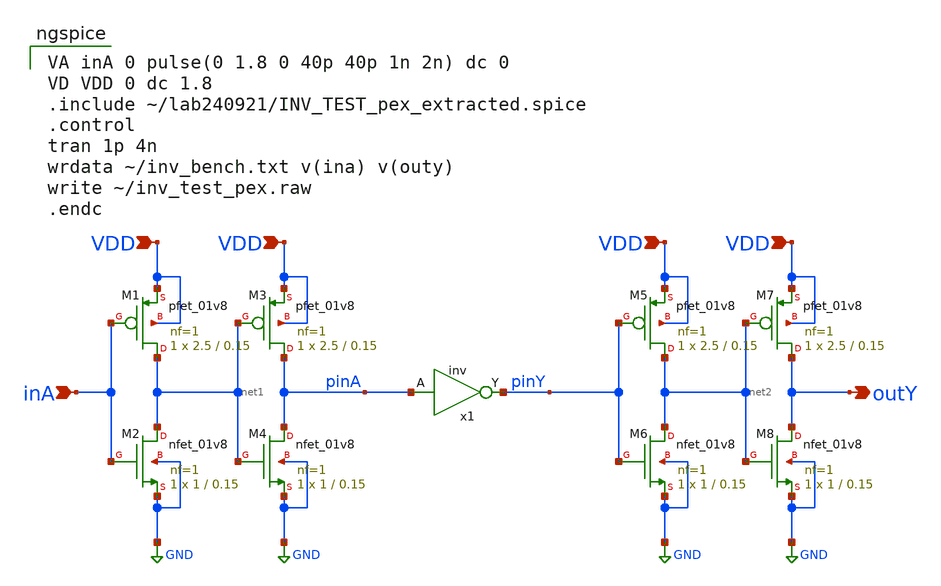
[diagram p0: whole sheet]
** sch_path: inv_pex.sch
**.subckt inv_pex inA VDD VDD VDD VDD outY
*.ipin inA
*.ipin VDD
*.ipin VDD
*.ipin VDD
*.ipin VDD
*.opin outY
XM1 net1 inA VDD VDD sky130_fd_pr__pfet_01v8 L=0.15 W=2.5 nf=1 ad='int((nf+1)/2) * W/nf * 0.29' as='int((nf+2)/2) * W/nf * 0.29'
+ pd='2*int((nf+1)/2) * (W/nf + 0.29)' ps='2*int((nf+2)/2) * (W/nf + 0.29)' nrd='0.29 / W' nrs='0.29 / W'
+ sa=0 sb=0 sd=0 mult=1 m=1
XM2 net1 inA GND GND sky130_fd_pr__nfet_01v8 L=0.15 W=1 nf=1 ad='int((nf+1)/2) * W/nf * 0.29' as='int((nf+2)/2) * W/nf * 0.29'
+ pd='2*int((nf+1)/2) * (W/nf + 0.29)' ps='2*int((nf+2)/2) * (W/nf + 0.29)' nrd='0.29 / W' nrs='0.29 / W'
+ sa=0 sb=0 sd=0 mult=1 m=1
x1 pinA pinY VDD GND INV_TEST
XM3 pinA net1 VDD VDD sky130_fd_pr__pfet_01v8 L=0.15 W=2.5 nf=1 ad='int((nf+1)/2) * W/nf * 0.29' as='int((nf+2)/2) * W/nf * 0.29'
+ pd='2*int((nf+1)/2) * (W/nf + 0.29)' ps='2*int((nf+2)/2) * (W/nf + 0.29)' nrd='0.29 / W' nrs='0.29 / W'
+ sa=0 sb=0 sd=0 mult=1 m=1
XM4 pinA net1 GND GND sky130_fd_pr__nfet_01v8 L=0.15 W=1 nf=1 ad='int((nf+1)/2) * W/nf * 0.29' as='int((nf+2)/2) * W/nf * 0.29'
+ pd='2*int((nf+1)/2) * (W/nf + 0.29)' ps='2*int((nf+2)/2) * (W/nf + 0.29)' nrd='0.29 / W' nrs='0.29 / W'
+ sa=0 sb=0 sd=0 mult=1 m=1
XM5 net2 pinY VDD VDD sky130_fd_pr__pfet_01v8 L=0.15 W=2.5 nf=1 ad='int((nf+1)/2) * W/nf * 0.29' as='int((nf+2)/2) * W/nf * 0.29'
+ pd='2*int((nf+1)/2) * (W/nf + 0.29)' ps='2*int((nf+2)/2) * (W/nf + 0.29)' nrd='0.29 / W' nrs='0.29 / W'
+ sa=0 sb=0 sd=0 mult=1 m=1
XM6 net2 pinY GND GND sky130_fd_pr__nfet_01v8 L=0.15 W=1 nf=1 ad='int((nf+1)/2) * W/nf * 0.29' as='int((nf+2)/2) * W/nf * 0.29'
+ pd='2*int((nf+1)/2) * (W/nf + 0.29)' ps='2*int((nf+2)/2) * (W/nf + 0.29)' nrd='0.29 / W' nrs='0.29 / W'
+ sa=0 sb=0 sd=0 mult=1 m=1
XM7 outY net2 VDD VDD sky130_fd_pr__pfet_01v8 L=0.15 W=2.5 nf=1 ad='int((nf+1)/2) * W/nf * 0.29' as='int((nf+2)/2) * W/nf * 0.29'
+ pd='2*int((nf+1)/2) * (W/nf + 0.29)' ps='2*int((nf+2)/2) * (W/nf + 0.29)' nrd='0.29 / W' nrs='0.29 / W'
+ sa=0 sb=0 sd=0 mult=1 m=1
XM8 outY net2 GND GND sky130_fd_pr__nfet_01v8 L=0.15 W=1 nf=1 ad='int((nf+1)/2) * W/nf * 0.29' as='int((nf+2)/2) * W/nf * 0.29'
+ pd='2*int((nf+1)/2) * (W/nf + 0.29)' ps='2*int((nf+2)/2) * (W/nf + 0.29)' nrd='0.29 / W' nrs='0.29 / W'
+ sa=0 sb=0 sd=0 mult=1 m=1
**** begin user architecture code

VA inA 0 pulse(0 1.8 0 40p 40p 1n 2n) dc 0
VD VDD 0 dc 1.8
.include ~/lab240921/INV_TEST_pex_extracted.spice
.control
tran 1p 4n
wrdata ~/inv_bench.txt v(ina) v(outy)
write ~/inv_test_pex.raw
.endc


** opencircuitdesign pdks install
.lib $::SKYWATER_MODELS/sky130.lib.spice ss


**** end user architecture code
**.ends
.GLOBAL GND
.end
